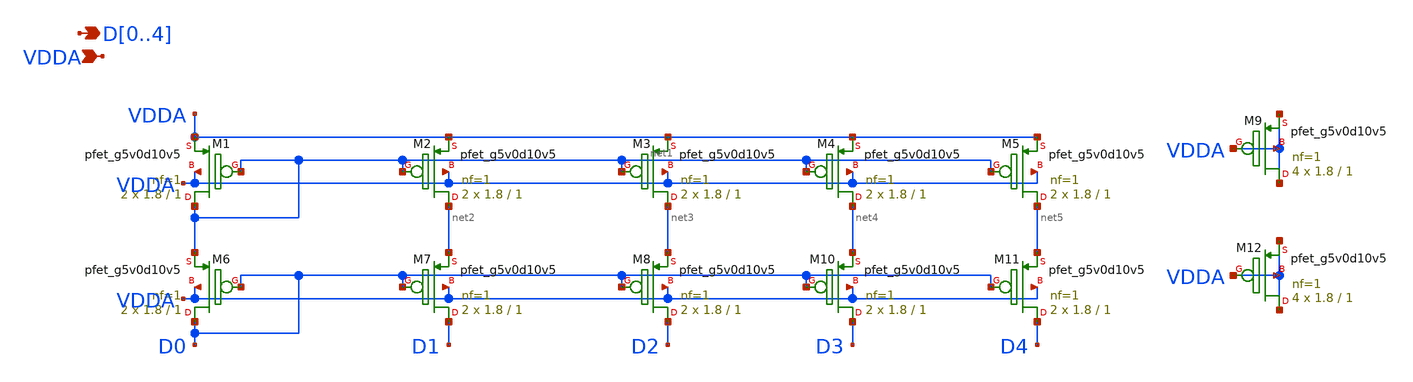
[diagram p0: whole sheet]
** sch_path: xschem/cm2_pcell.sch
**.subckt cm2_pcell D0,D1,D2,D3,D4 VDDA
*.opin D0,D1,D2,D3,D4
*.ipin VDDA
XM1 net1 net1 VDDA VDDA sky130_fd_pr__pfet_g5v0d10v5 L=1 W=1.8 nf=1 ad='int((nf+1)/2) * W/nf * 0.29'
+ as='int((nf+2)/2) * W/nf * 0.29' pd='2*int((nf+1)/2) * (W/nf + 0.29)' ps='2*int((nf+2)/2) * (W/nf + 0.29)'
+ nrd='0.29 / W' nrs='0.29 / W' sa=0 sb=0 sd=0 mult=2 m=2
XM9 VDDA VDDA VDDA VDDA sky130_fd_pr__pfet_g5v0d10v5 L=1 W=1.8 nf=1 ad='int((nf+1)/2) * W/nf * 0.29'
+ as='int((nf+2)/2) * W/nf * 0.29' pd='2*int((nf+1)/2) * (W/nf + 0.29)' ps='2*int((nf+2)/2) * (W/nf + 0.29)'
+ nrd='0.29 / W' nrs='0.29 / W' sa=0 sb=0 sd=0 mult=4 m=4
XM2 net2 net1 VDDA VDDA sky130_fd_pr__pfet_g5v0d10v5 L=1 W=1.8 nf=1 ad='int((nf+1)/2) * W/nf * 0.29'
+ as='int((nf+2)/2) * W/nf * 0.29' pd='2*int((nf+1)/2) * (W/nf + 0.29)' ps='2*int((nf+2)/2) * (W/nf + 0.29)'
+ nrd='0.29 / W' nrs='0.29 / W' sa=0 sb=0 sd=0 mult=2 m=2
XM3 net3 net1 VDDA VDDA sky130_fd_pr__pfet_g5v0d10v5 L=1 W=1.8 nf=1 ad='int((nf+1)/2) * W/nf * 0.29'
+ as='int((nf+2)/2) * W/nf * 0.29' pd='2*int((nf+1)/2) * (W/nf + 0.29)' ps='2*int((nf+2)/2) * (W/nf + 0.29)'
+ nrd='0.29 / W' nrs='0.29 / W' sa=0 sb=0 sd=0 mult=2 m=2
XM4 net4 net1 VDDA VDDA sky130_fd_pr__pfet_g5v0d10v5 L=1 W=1.8 nf=1 ad='int((nf+1)/2) * W/nf * 0.29'
+ as='int((nf+2)/2) * W/nf * 0.29' pd='2*int((nf+1)/2) * (W/nf + 0.29)' ps='2*int((nf+2)/2) * (W/nf + 0.29)'
+ nrd='0.29 / W' nrs='0.29 / W' sa=0 sb=0 sd=0 mult=2 m=2
XM5 net5 net1 VDDA VDDA sky130_fd_pr__pfet_g5v0d10v5 L=1 W=1.8 nf=1 ad='int((nf+1)/2) * W/nf * 0.29'
+ as='int((nf+2)/2) * W/nf * 0.29' pd='2*int((nf+1)/2) * (W/nf + 0.29)' ps='2*int((nf+2)/2) * (W/nf + 0.29)'
+ nrd='0.29 / W' nrs='0.29 / W' sa=0 sb=0 sd=0 mult=2 m=2
XM6 D0 D0 net1 VDDA sky130_fd_pr__pfet_g5v0d10v5 L=1 W=1.8 nf=1 ad='int((nf+1)/2) * W/nf * 0.29' as='int((nf+2)/2) * W/nf * 0.29'
+ pd='2*int((nf+1)/2) * (W/nf + 0.29)' ps='2*int((nf+2)/2) * (W/nf + 0.29)' nrd='0.29 / W' nrs='0.29 / W'
+ sa=0 sb=0 sd=0 mult=2 m=2
XM7 D1 D0 net2 VDDA sky130_fd_pr__pfet_g5v0d10v5 L=1 W=1.8 nf=1 ad='int((nf+1)/2) * W/nf * 0.29' as='int((nf+2)/2) * W/nf * 0.29'
+ pd='2*int((nf+1)/2) * (W/nf + 0.29)' ps='2*int((nf+2)/2) * (W/nf + 0.29)' nrd='0.29 / W' nrs='0.29 / W'
+ sa=0 sb=0 sd=0 mult=2 m=2
XM8 D2 D0 net3 VDDA sky130_fd_pr__pfet_g5v0d10v5 L=1 W=1.8 nf=1 ad='int((nf+1)/2) * W/nf * 0.29' as='int((nf+2)/2) * W/nf * 0.29'
+ pd='2*int((nf+1)/2) * (W/nf + 0.29)' ps='2*int((nf+2)/2) * (W/nf + 0.29)' nrd='0.29 / W' nrs='0.29 / W'
+ sa=0 sb=0 sd=0 mult=2 m=2
XM10 D3 D0 net4 VDDA sky130_fd_pr__pfet_g5v0d10v5 L=1 W=1.8 nf=1 ad='int((nf+1)/2) * W/nf * 0.29' as='int((nf+2)/2) * W/nf * 0.29'
+ pd='2*int((nf+1)/2) * (W/nf + 0.29)' ps='2*int((nf+2)/2) * (W/nf + 0.29)' nrd='0.29 / W' nrs='0.29 / W'
+ sa=0 sb=0 sd=0 mult=2 m=2
XM11 D4 D0 net5 VDDA sky130_fd_pr__pfet_g5v0d10v5 L=1 W=1.8 nf=1 ad='int((nf+1)/2) * W/nf * 0.29' as='int((nf+2)/2) * W/nf * 0.29'
+ pd='2*int((nf+1)/2) * (W/nf + 0.29)' ps='2*int((nf+2)/2) * (W/nf + 0.29)' nrd='0.29 / W' nrs='0.29 / W'
+ sa=0 sb=0 sd=0 mult=2 m=2
XM12 VDDA VDDA VDDA VDDA sky130_fd_pr__pfet_g5v0d10v5 L=1 W=1.8 nf=1 ad='int((nf+1)/2) * W/nf * 0.29'
+ as='int((nf+2)/2) * W/nf * 0.29' pd='2*int((nf+1)/2) * (W/nf + 0.29)' ps='2*int((nf+2)/2) * (W/nf + 0.29)'
+ nrd='0.29 / W' nrs='0.29 / W' sa=0 sb=0 sd=0 mult=4 m=4
**.ends
.end
